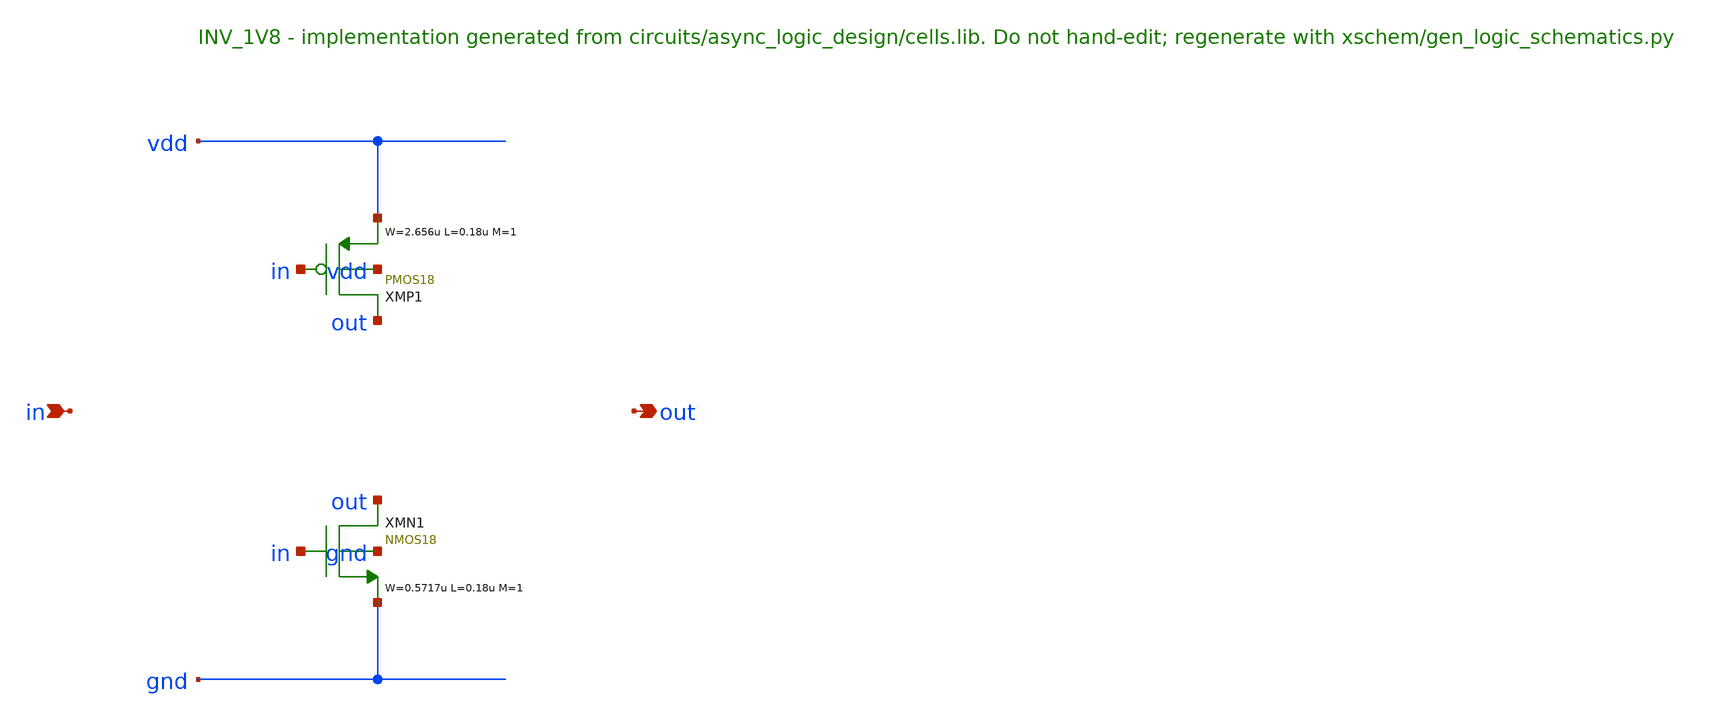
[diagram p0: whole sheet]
** sch_path: xschem/logic/INV_1V8.sch
**.subckt INV_1V8 in out
*.ipin in
*.opin out
XMP1 out in vdd vdd PMOS18 W=2.656u L=0.18u M=1 MM_SIGMA=0
XMN1 out in gnd gnd NMOS18 W=0.5717u L=0.18u M=1 MM_SIGMA=0
**.ends
.end
